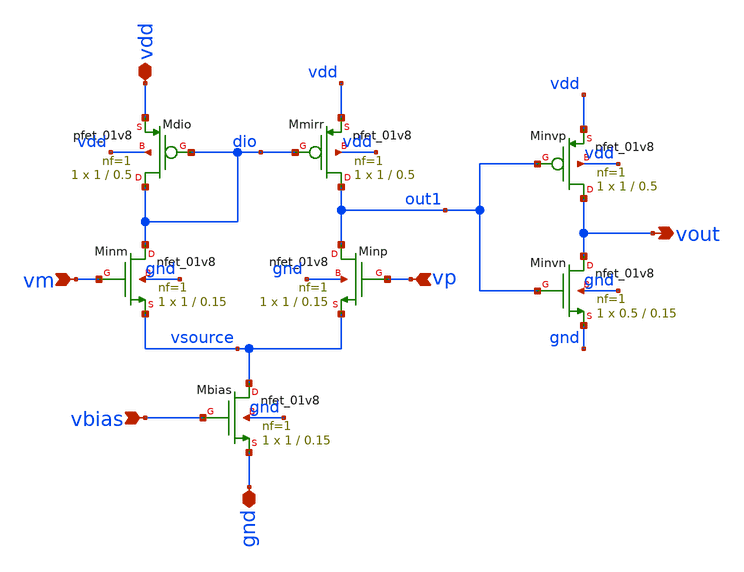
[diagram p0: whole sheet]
** sch_path: analog/klayout/production/final_merge_20260923/testbenches/cace/analog/xschem/amp_comp.sch
**.subckt amp_comp vdd gnd vbias vm vp vout
*.iopin vdd
*.iopin gnd
*.ipin vbias
*.ipin vm
*.ipin vp
*.opin vout
XMmirr out1 dio vdd vdd sky130_fd_pr__pfet_01v8 L=0.5 W=1 nf=1 ad='int((1 + 1)/2) * 1 / 1 * 0.29' as='int((1 + 2)/2) * 1 / 1 * 0.29'
+ pd='2*int((1 + 1)/2) * (1 / 1 + 0.29)' ps='2*int((1 + 2)/2) * (1 / 1 + 0.29)' nrd='0.29 / 1 ' nrs='0.29 / 1 '
+ sa=0 sb=0 sd=0 mult=1 m=1
XMdio dio dio vdd vdd sky130_fd_pr__pfet_01v8 L=0.5 W=1 nf=1 ad='int((1 + 1)/2) * 1 / 1 * 0.29' as='int((1 + 2)/2) * 1 / 1 * 0.29'
+ pd='2*int((1 + 1)/2) * (1 / 1 + 0.29)' ps='2*int((1 + 2)/2) * (1 / 1 + 0.29)' nrd='0.29 / 1 ' nrs='0.29 / 1 '
+ sa=0 sb=0 sd=0 mult=1 m=1
XMinm dio vm vsource gnd sky130_fd_pr__nfet_01v8 L=0.15 W=1 nf=1 ad='int((1 + 1)/2) * 1 / 1 * 0.29' as='int((1 + 2)/2) * 1 / 1 * 0.29'
+ pd='2*int((1 + 1)/2) * (1 / 1 + 0.29)' ps='2*int((1 + 2)/2) * (1 / 1 + 0.29)' nrd='0.29 / 1 ' nrs='0.29 / 1 '
+ sa=0 sb=0 sd=0 mult=1 m=1
XMinp out1 vp vsource gnd sky130_fd_pr__nfet_01v8 L=0.15 W=1 nf=1 ad='int((1 + 1)/2) * 1 / 1 * 0.29'
+ as='int((1 + 2)/2) * 1 / 1 * 0.29' pd='2*int((1 + 1)/2) * (1 / 1 + 0.29)' ps='2*int((1 + 2)/2) * (1 / 1 + 0.29)'
+ nrd='0.29 / 1 ' nrs='0.29 / 1 ' sa=0 sb=0 sd=0 mult=1 m=1
XMinvn vout out1 gnd gnd sky130_fd_pr__nfet_01v8 L=0.15 W=0.5 nf=1 ad='int((1 + 1)/2) * 0.5 / 1 * 0.29'
+ as='int((1 + 2)/2) * 0.5 / 1 * 0.29' pd='2*int((1 + 1)/2) * (0.5 / 1 + 0.29)' ps='2*int((1 + 2)/2) * (0.5 / 1 + 0.29)'
+ nrd='0.29 / 0.5 ' nrs='0.29 / 0.5 ' sa=0 sb=0 sd=0 mult=1 m=1
XMinvp vout out1 vdd vdd sky130_fd_pr__pfet_01v8 L=0.5 W=1 nf=1 ad='int((1 + 1)/2) * 1 / 1 * 0.29' as='int((1 + 2)/2) * 1 / 1 * 0.29'
+ pd='2*int((1 + 1)/2) * (1 / 1 + 0.29)' ps='2*int((1 + 2)/2) * (1 / 1 + 0.29)' nrd='0.29 / 1 ' nrs='0.29 / 1 '
+ sa=0 sb=0 sd=0 mult=1 m=1
XMbias vsource vbias gnd gnd sky130_fd_pr__nfet_01v8 L=0.15 W=1 nf=1 ad='int((1 + 1)/2) * 1 / 1 * 0.29'
+ as='int((1 + 2)/2) * 1 / 1 * 0.29' pd='2*int((1 + 1)/2) * (1 / 1 + 0.29)' ps='2*int((1 + 2)/2) * (1 / 1 + 0.29)'
+ nrd='0.29 / 1 ' nrs='0.29 / 1 ' sa=0 sb=0 sd=0 mult=1 m=1
**.ends
.end
